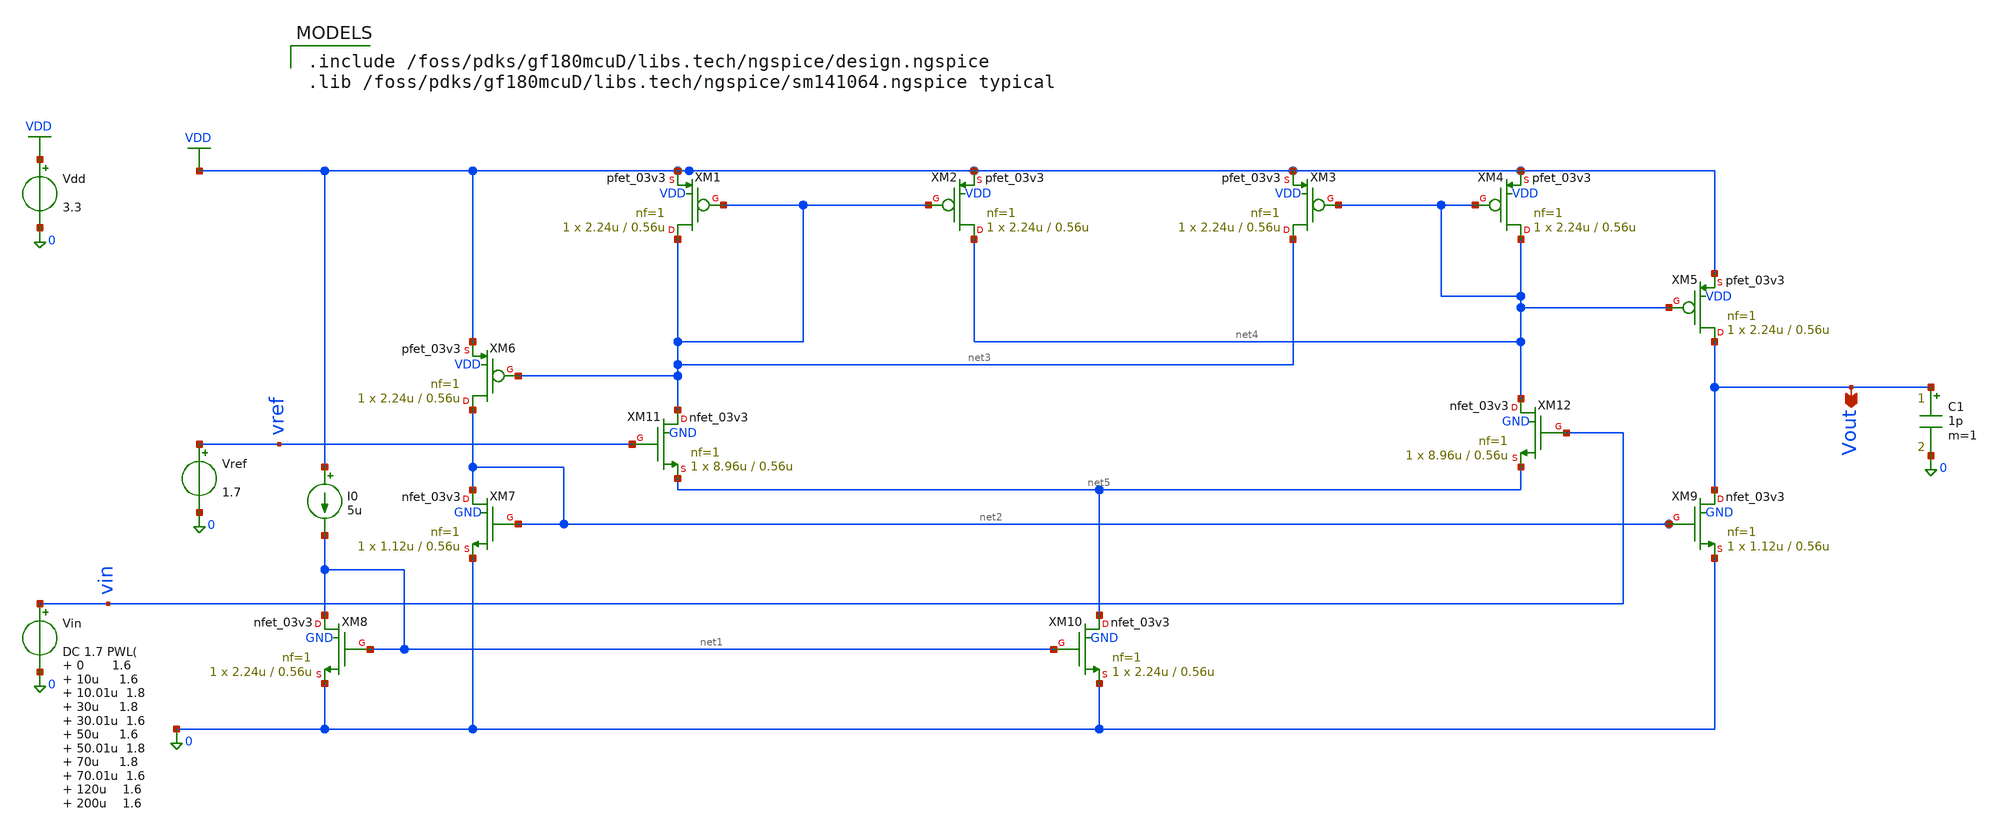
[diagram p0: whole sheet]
** sch_path: comparator/schematic-design/comp.sch
**.subckt comp Vout
*.opin Vout
XM1 net3 net3 VDD VDD pfet_03v3 L=0.56u W=2.24u nf=1 ad='int((nf+1)/2) * W/nf * 0.18u' as='int((nf+2)/2) * W/nf * 0.18u'
+ pd='2*int((nf+1)/2) * (W/nf + 0.18u)' ps='2*int((nf+2)/2) * (W/nf + 0.18u)' nrd='0.18u / W' nrs='0.18u / W'
+ sa=0 sb=0 sd=0 m=1 par=1
XM2 net4 net3 VDD VDD pfet_03v3 L=0.56u W=2.24u nf=1 ad='int((nf+1)/2) * W/nf * 0.18u' as='int((nf+2)/2) * W/nf * 0.18u'
+ pd='2*int((nf+1)/2) * (W/nf + 0.18u)' ps='2*int((nf+2)/2) * (W/nf + 0.18u)' nrd='0.18u / W' nrs='0.18u / W'
+ sa=0 sb=0 sd=0 m=1 par=1
XM3 net3 net4 VDD VDD pfet_03v3 L=0.56u W=2.24u nf=1 ad='int((nf+1)/2) * W/nf * 0.18u' as='int((nf+2)/2) * W/nf * 0.18u'
+ pd='2*int((nf+1)/2) * (W/nf + 0.18u)' ps='2*int((nf+2)/2) * (W/nf + 0.18u)' nrd='0.18u / W' nrs='0.18u / W'
+ sa=0 sb=0 sd=0 m=1 par=1
XM4 net4 net4 VDD VDD pfet_03v3 L=0.56u W=2.24u nf=1 ad='int((nf+1)/2) * W/nf * 0.18u' as='int((nf+2)/2) * W/nf * 0.18u'
+ pd='2*int((nf+1)/2) * (W/nf + 0.18u)' ps='2*int((nf+2)/2) * (W/nf + 0.18u)' nrd='0.18u / W' nrs='0.18u / W'
+ sa=0 sb=0 sd=0 m=1 par=1
XM5 Vout net4 VDD VDD pfet_03v3 L=0.56u W=2.24u nf=1 ad='int((nf+1)/2) * W/nf * 0.18u' as='int((nf+2)/2) * W/nf * 0.18u'
+ pd='2*int((nf+1)/2) * (W/nf + 0.18u)' ps='2*int((nf+2)/2) * (W/nf + 0.18u)' nrd='0.18u / W' nrs='0.18u / W'
+ sa=0 sb=0 sd=0 m=1 par=1
XM6 net2 net3 VDD VDD pfet_03v3 L=0.56u W=2.24u nf=1 ad='int((nf+1)/2) * W/nf * 0.18u' as='int((nf+2)/2) * W/nf * 0.18u'
+ pd='2*int((nf+1)/2) * (W/nf + 0.18u)' ps='2*int((nf+2)/2) * (W/nf + 0.18u)' nrd='0.18u / W' nrs='0.18u / W'
+ sa=0 sb=0 sd=0 m=1 par=1
XM7 net2 net2 0 GND nfet_03v3 L=0.56u W=1.12u nf=1 ad='int((nf+1)/2) * W/nf * 0.18u' as='int((nf+2)/2) * W/nf * 0.18u'
+ pd='2*int((nf+1)/2) * (W/nf + 0.18u)' ps='2*int((nf+2)/2) * (W/nf + 0.18u)' nrd='0.18u / W' nrs='0.18u / W'
+ sa=0 sb=0 sd=0 m=1 par=1
XM8 net1 net1 0 GND nfet_03v3 L=0.56u W=2.24u nf=1 ad='int((nf+1)/2) * W/nf * 0.18u' as='int((nf+2)/2) * W/nf * 0.18u'
+ pd='2*int((nf+1)/2) * (W/nf + 0.18u)' ps='2*int((nf+2)/2) * (W/nf + 0.18u)' nrd='0.18u / W' nrs='0.18u / W'
+ sa=0 sb=0 sd=0 m=1 par=1
XM9 Vout net2 0 GND nfet_03v3 L=0.56u W=1.12u nf=1 ad='int((nf+1)/2) * W/nf * 0.18u' as='int((nf+2)/2) * W/nf * 0.18u'
+ pd='2*int((nf+1)/2) * (W/nf + 0.18u)' ps='2*int((nf+2)/2) * (W/nf + 0.18u)' nrd='0.18u / W' nrs='0.18u / W'
+ sa=0 sb=0 sd=0 m=1 par=1
XM10 net5 net1 0 GND nfet_03v3 L=0.56u W=2.24u nf=1 ad='int((nf+1)/2) * W/nf * 0.18u' as='int((nf+2)/2) * W/nf * 0.18u'
+ pd='2*int((nf+1)/2) * (W/nf + 0.18u)' ps='2*int((nf+2)/2) * (W/nf + 0.18u)' nrd='0.18u / W' nrs='0.18u / W'
+ sa=0 sb=0 sd=0 m=1 par=1
XM11 net3 vref net5 GND nfet_03v3 L=0.56u W=8.96u nf=1 ad='int((nf+1)/2) * W/nf * 0.18u' as='int((nf+2)/2) * W/nf * 0.18u'
+ pd='2*int((nf+1)/2) * (W/nf + 0.18u)' ps='2*int((nf+2)/2) * (W/nf + 0.18u)' nrd='0.18u / W' nrs='0.18u / W'
+ sa=0 sb=0 sd=0 m=1 par=1
XM12 net4 vin net5 GND nfet_03v3 L=0.56u W=8.96u nf=1 ad='int((nf+1)/2) * W/nf * 0.18u' as='int((nf+2)/2) * W/nf * 0.18u'
+ pd='2*int((nf+1)/2) * (W/nf + 0.18u)' ps='2*int((nf+2)/2) * (W/nf + 0.18u)' nrd='0.18u / W' nrs='0.18u / W'
+ sa=0 sb=0 sd=0 m=1 par=1
I0 VDD net1 5u
Vref vref 0 1.7
Vin vin 0 DC 1.7 PWL( 0 1.6 10u 1.6 10.01u 1.8 30u 1.8 30.01u 1.6 50u 1.6 50.01u 1.8 70u 1.8 70.01u
+ 1.6 120u 1.6 200u 1.6 300u 1.8 400u 1.6 420u 1.6
)

Vdd VDD 0 3.3
C1 Vout 0 1p m=1
**** begin user architecture code

.include /foss/pdks/gf180mcuD/libs.tech/ngspice/design.ngspice
.lib /foss/pdks/gf180mcuD/libs.tech/ngspice/sm141064.ngspice typical


.control
set noaskquit

save all

save @m.xm1.m0[gm]
save @m.xm1.m0[id]

save @m.xm2.m0[gm]
save @m.xm2.m0[id]

save @m.xm3.m0[gm]
save @m.xm3.m0[id]

save @m.xm4.m0[gm]
save @m.xm4.m0[id]

save @m.xm5.m0[gm]
save @m.xm5.m0[id]

save @m.xm6.m0[gm]
save @m.xm6.m0[id]

save @m.xm7.m0[gm]
save @m.xm7.m0[id]

save @m.xm8.m0[gm]
save @m.xm8.m0[id]

save @m.xm9.m0[gm]
save @m.xm9.m0[id]

save @m.xm10.m0[gm]
save @m.xm10.m0[id]

save @m.xm11.m0[gm]
save @m.xm11.m0[id]

save @m.xm12.m0[gm]
save @m.xm12.m0[id]

op
write comparator_op.raw

.endc

**** end user architecture code
**.ends
.GLOBAL VDD
.end
